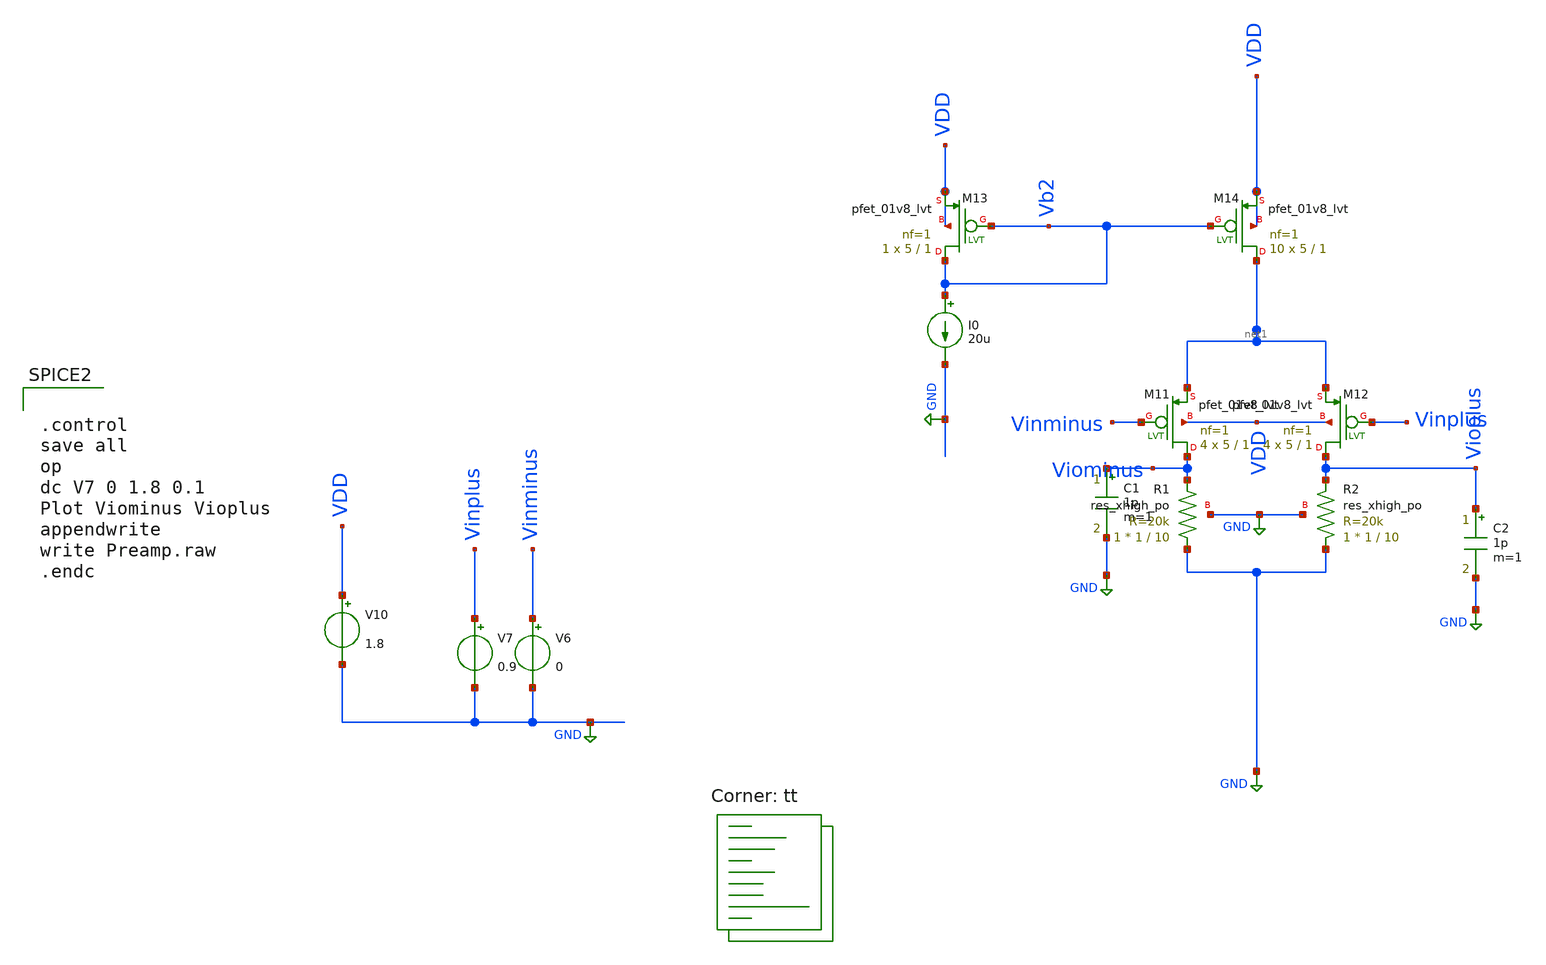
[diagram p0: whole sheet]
** sch_path: xschem/Amplifiers/Preamp.sch
**.subckt Preamp
XR1 GND Viominus GND sky130_fd_pr__res_xhigh_po W=1 L=10 mult=1 m=1
XR2 GND Vioplus GND sky130_fd_pr__res_xhigh_po W=1 L=10 mult=1 m=1
I0 Vb2 GND 20u
XM11 Viominus Vinminus net1 VDD sky130_fd_pr__pfet_01v8_lvt L=1 W=5 nf=1 ad='int((nf+1)/2) * W/nf * 0.29'
+ as='int((nf+2)/2) * W/nf * 0.29' pd='2*int((nf+1)/2) * (W/nf + 0.29)' ps='2*int((nf+2)/2) * (W/nf + 0.29)'
+ nrd='0.29 / W' nrs='0.29 / W' sa=0 sb=0 sd=0 mult=4 m=4
XM12 Vioplus Vinplus net1 VDD sky130_fd_pr__pfet_01v8_lvt L=1 W=5 nf=1 ad='int((nf+1)/2) * W/nf * 0.29'
+ as='int((nf+2)/2) * W/nf * 0.29' pd='2*int((nf+1)/2) * (W/nf + 0.29)' ps='2*int((nf+2)/2) * (W/nf + 0.29)'
+ nrd='0.29 / W' nrs='0.29 / W' sa=0 sb=0 sd=0 mult=4 m=4
XM13 Vb2 Vb2 VDD VDD sky130_fd_pr__pfet_01v8_lvt L=1 W=5 nf=1 ad='int((nf+1)/2) * W/nf * 0.29' as='int((nf+2)/2) * W/nf * 0.29'
+ pd='2*int((nf+1)/2) * (W/nf + 0.29)' ps='2*int((nf+2)/2) * (W/nf + 0.29)' nrd='0.29 / W' nrs='0.29 / W'
+ sa=0 sb=0 sd=0 mult=1 m=1
XM14 net1 Vb2 VDD VDD sky130_fd_pr__pfet_01v8_lvt L=1 W=5 nf=1 ad='int((nf+1)/2) * W/nf * 0.29' as='int((nf+2)/2) * W/nf * 0.29'
+ pd='2*int((nf+1)/2) * (W/nf + 0.29)' ps='2*int((nf+2)/2) * (W/nf + 0.29)' nrd='0.29 / W' nrs='0.29 / W'
+ sa=0 sb=0 sd=0 mult=10 m=10
V6 Vinminus GND 0
.save i(v6)
V7 Vinplus GND 0.9
.save i(v7)
V10 VDD GND 1.8
.save i(v10)
C1 Viominus GND 1p m=1
C2 Vioplus GND 1p m=1
**** begin user architecture code


.control
save all
op
dc V7 0 1.8 0.1
Plot Viominus Vioplus
appendwrite
write Preamp.raw
.endc


.lib $::SKYWATER_MODELS/sky130.lib.spice tt
**** end user architecture code
**.ends
.GLOBAL GND
.end
